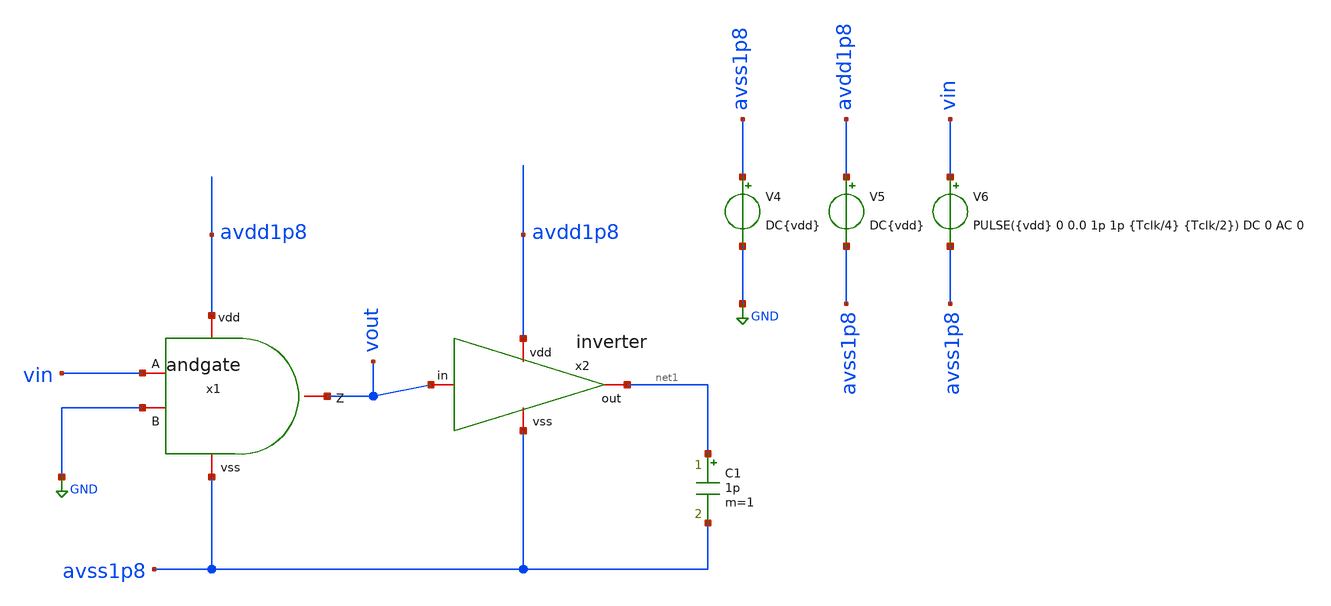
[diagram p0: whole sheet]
** sch_path: verification/testbenches/andgate/tb_andgate.sch
**.subckt tb_andgate
C1 net1 avss1p8 1p m=1
V4 avss1p8 GND DC{vdd}
V5 avdd1p8 avss1p8 DC{vdd}
V6 vin avss1p8 PULSE({vdd} 0 0.0 1p 1p {Tclk/4} {Tclk/2}) DC 0 AC 0
x1 avdd1p8 vin GND vout avss1p8 andgate
x2 avdd1p8 vout net1 avss1p8 inverter
**** begin user architecture code


* Circuit Parameters
.param vdd = 1
.param vss = 0.0
.param Tclk = 10n
.options TEMP = 27.0
* Include Models - IHP SG13G2
.lib cornerMOSlv.lib mos_tt
* OP Parameters & Singals to save
.save all
*Simulations
.control
tran 0.01u 100n
setplot tran1
plot v(vin) v(vout)+1
reset
dc V6 0 1 0.01
setplot dc
plot vin vout ylabel vout xlabel vin
set filetype = ascii
write dcsweep.raw
.endc
.end


**** end user architecture code
**.ends

* expanding   symbol:  blocks/andgate/schematic/andgate.sym # of pins=5
** sym_path: design/blocks/andgate/schematic/andgate.sym
** sch_path: design/blocks/andgate/schematic/andgate.sch
.subckt andgate vdd A B Z vss
*.iopin A
*.iopin vdd
*.iopin vss
*.iopin B
*.iopin Z
XM1 net1 A vdd vdd sg13_lv_pmos w=1.0u l=0.72u ng=1 m=1 rfmode=1 mm_ok=1
XM2 vdd B net1 vdd sg13_lv_pmos w=1.0u l=0.72u ng=1 m=1 rfmode=1 mm_ok=1
XM3 net1 A net2 vss sg13_lv_nmos w=1.0u l=0.72u ng=1 m=1 rfmode=1 mm_ok=1
XM4 net2 B vss vss sg13_lv_nmos w=1.0u l=0.72u ng=1 m=1 rfmode=1 mm_ok=1
XM5 Z net1 vdd vdd sg13_lv_pmos w=1.0u l=0.72u ng=1 m=1 rfmode=1 mm_ok=1
XM6 Z net1 vss vss sg13_lv_nmos w=1.0u l=0.72u ng=1 m=1 rfmode=1 mm_ok=1
.ends


* expanding   symbol:  blocks/inverter/schematic/inverter.sym # of pins=4
** sym_path: design/blocks/inverter/schematic/inverter.sym
** sch_path: design/blocks/inverter/schematic/inverter.sch
.subckt inverter vdd in out vss
*.iopin in
*.iopin out
*.iopin vss
*.iopin vdd
XM1 out in vdd vdd sg13_lv_pmos w=0.15u l=0.13u ng=1 m=1 mm_ok=1
XM2 out in vss vss sg13_lv_nmos w=0.15u l=0.13u ng=1 m=1 mm_ok=1
.ends

.GLOBAL GND
.end
